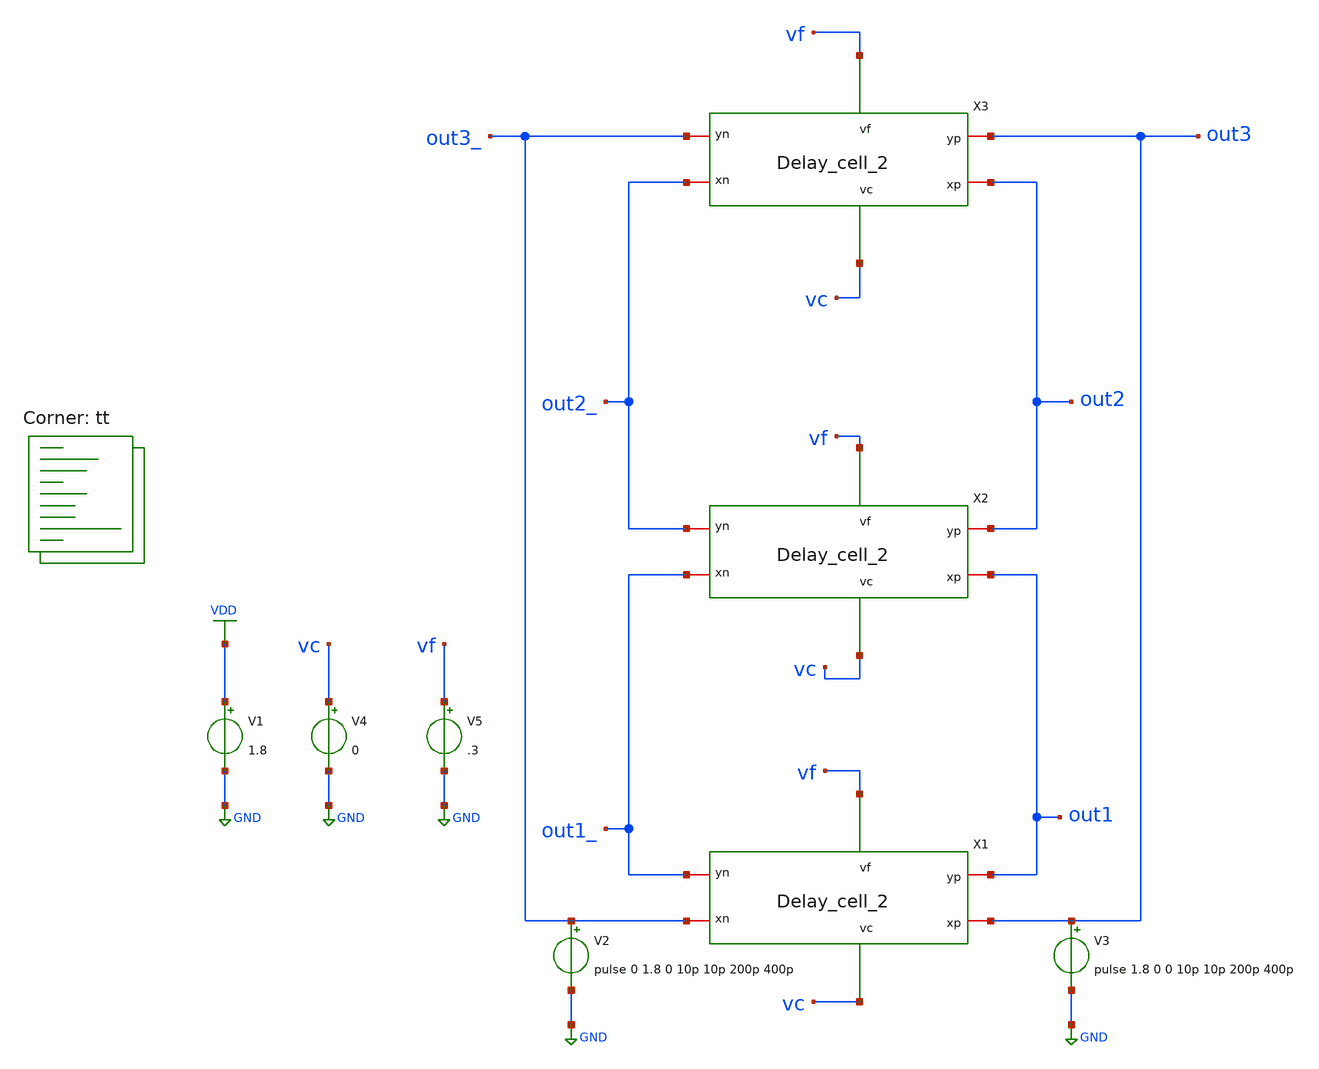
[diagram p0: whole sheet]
** sch_path: RO2.sch
**.subckt RO2
V1 VDD GND 1.8
X1 out1 out1_ out3 out3_ vf vc Delay_cell_2
X3 out3 out3_ out2 out2_ vf vc Delay_cell_2
V2 out3_ GND pulse 0 1.8 0 10p 10p 200p 400p
V3 out3 GND pulse 1.8 0 0 10p 10p 200p 400p
X2 out2 out2_ out1 out1_ vf vc Delay_cell_2
V4 vc GND 0
V5 vf GND .3
**** begin user architecture code



.tran .1p 10n
.probe I(x1)
.save all

.lib $::SKYWATER_MODELS/sky130.lib.spice tt
**** end user architecture code
**.ends

* expanding   symbol:  Delay_cell_2.sym # of pins=6
** sym_path: Delay_cell_2.sym
** sch_path: Delay_cell_2.sch
.subckt Delay_cell_2 yp yn xp xn vf vc
*.iopin yp
*.iopin xn
*.iopin xp
*.iopin yn
*.ipin vf
*.ipin vc
R2 yp net1 800 m=1
R1 yn net2 800 m=1
XM1 net1 xn GND GND sky130_fd_pr__nfet_01v8 L=0.15 W=2.6 nf=1 ad='int((nf+1)/2) * W/nf * 0.29' as='int((nf+2)/2) * W/nf * 0.29'
+ pd='2*int((nf+1)/2) * (W/nf + 0.29)' ps='2*int((nf+2)/2) * (W/nf + 0.29)' nrd='0.29 / W' nrs='0.29 / W'
+ sa=0 sb=0 sd=0 mult=1 m=1
XM2 net2 xp GND GND sky130_fd_pr__nfet_01v8 L=0.15 W=2.6 nf=1 ad='int((nf+1)/2) * W/nf * 0.29' as='int((nf+2)/2) * W/nf * 0.29'
+ pd='2*int((nf+1)/2) * (W/nf + 0.29)' ps='2*int((nf+2)/2) * (W/nf + 0.29)' nrd='0.29 / W' nrs='0.29 / W'
+ sa=0 sb=0 sd=0 mult=1 m=1
XM3 yn net1 VDD VDD sky130_fd_pr__pfet_01v8 L=0.15 W=1 nf=1 ad='int((nf+1)/2) * W/nf * 0.29' as='int((nf+2)/2) * W/nf * 0.29'
+ pd='2*int((nf+1)/2) * (W/nf + 0.29)' ps='2*int((nf+2)/2) * (W/nf + 0.29)' nrd='0.29 / W' nrs='0.29 / W'
+ sa=0 sb=0 sd=0 mult=1 m=1
XM4 yp vf VDD VDD sky130_fd_pr__pfet_01v8 L=0.15 W=.6 nf=1 ad='int((nf+1)/2) * W/nf * 0.29' as='int((nf+2)/2) * W/nf * 0.29'
+ pd='2*int((nf+1)/2) * (W/nf + 0.29)' ps='2*int((nf+2)/2) * (W/nf + 0.29)' nrd='0.29 / W' nrs='0.29 / W'
+ sa=0 sb=0 sd=0 mult=1 m=1
XM5 yp vc VDD VDD sky130_fd_pr__pfet_01v8 L=0.15 W=1 nf=1 ad='int((nf+1)/2) * W/nf * 0.29' as='int((nf+2)/2) * W/nf * 0.29'
+ pd='2*int((nf+1)/2) * (W/nf + 0.29)' ps='2*int((nf+2)/2) * (W/nf + 0.29)' nrd='0.29 / W' nrs='0.29 / W'
+ sa=0 sb=0 sd=0 mult=1 m=1
XM6 yp net2 VDD VDD sky130_fd_pr__pfet_01v8 L=0.15 W=1 nf=1 ad='int((nf+1)/2) * W/nf * 0.29' as='int((nf+2)/2) * W/nf * 0.29'
+ pd='2*int((nf+1)/2) * (W/nf + 0.29)' ps='2*int((nf+2)/2) * (W/nf + 0.29)' nrd='0.29 / W' nrs='0.29 / W'
+ sa=0 sb=0 sd=0 mult=1 m=1
XM7 yn vf VDD VDD sky130_fd_pr__pfet_01v8 L=0.15 W=.6 nf=1 ad='int((nf+1)/2) * W/nf * 0.29' as='int((nf+2)/2) * W/nf * 0.29'
+ pd='2*int((nf+1)/2) * (W/nf + 0.29)' ps='2*int((nf+2)/2) * (W/nf + 0.29)' nrd='0.29 / W' nrs='0.29 / W'
+ sa=0 sb=0 sd=0 mult=1 m=1
XM8 yn vc VDD VDD sky130_fd_pr__pfet_01v8 L=0.15 W=1 nf=1 ad='int((nf+1)/2) * W/nf * 0.29' as='int((nf+2)/2) * W/nf * 0.29'
+ pd='2*int((nf+1)/2) * (W/nf + 0.29)' ps='2*int((nf+2)/2) * (W/nf + 0.29)' nrd='0.29 / W' nrs='0.29 / W'
+ sa=0 sb=0 sd=0 mult=1 m=1
.ends

.GLOBAL VDD
.GLOBAL GND
.end
